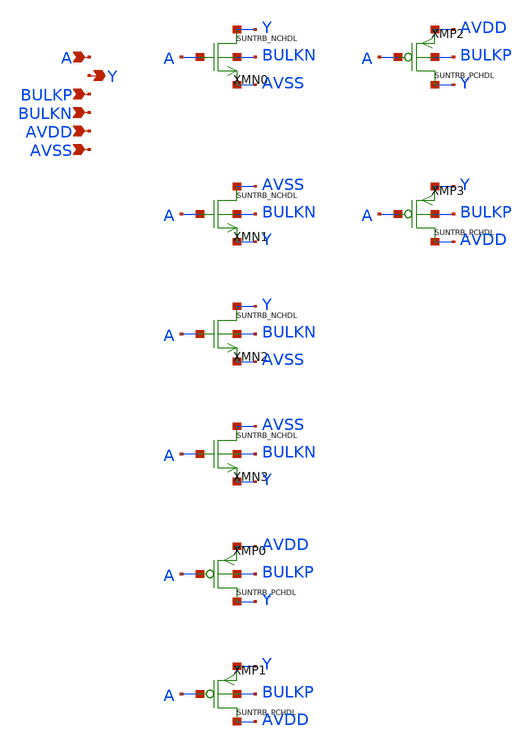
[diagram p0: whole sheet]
** sch_path: design/SUN_TRB_SKY130NM/SUNTRB_IVX4_CV.sch
**.subckt SUNTRB_IVX4_CV A Y BULKP BULKN AVDD AVSS
*.ipin A
*.opin Y
*.ipin BULKP
*.ipin BULKN
*.ipin AVDD
*.ipin AVSS
XMN0 Y A AVSS BULKN SUNTRB_NCHDL xoffset=0 yoffset=0 angle=0
XMN1 AVSS A Y BULKN SUNTRB_NCHDL xoffset=0 yoffset=0 angle=0
XMN2 Y A AVSS BULKN SUNTRB_NCHDL xoffset=0 yoffset=0 angle=0
XMN3 AVSS A Y BULKN SUNTRB_NCHDL xoffset=0 yoffset=0 angle=0
XMP0 Y A AVDD BULKP SUNTRB_PCHDL xoffset=0 yoffset=0 angle=0 M=1
XMP1 AVDD A Y BULKP SUNTRB_PCHDL xoffset=0 yoffset=0 angle=0 M=1
XMP2 Y A AVDD BULKP SUNTRB_PCHDL xoffset=0 yoffset=0 angle=0 M=1
XMP3 AVDD A Y BULKP SUNTRB_PCHDL xoffset=0 yoffset=0 angle=0 M=1
**.ends
.end
